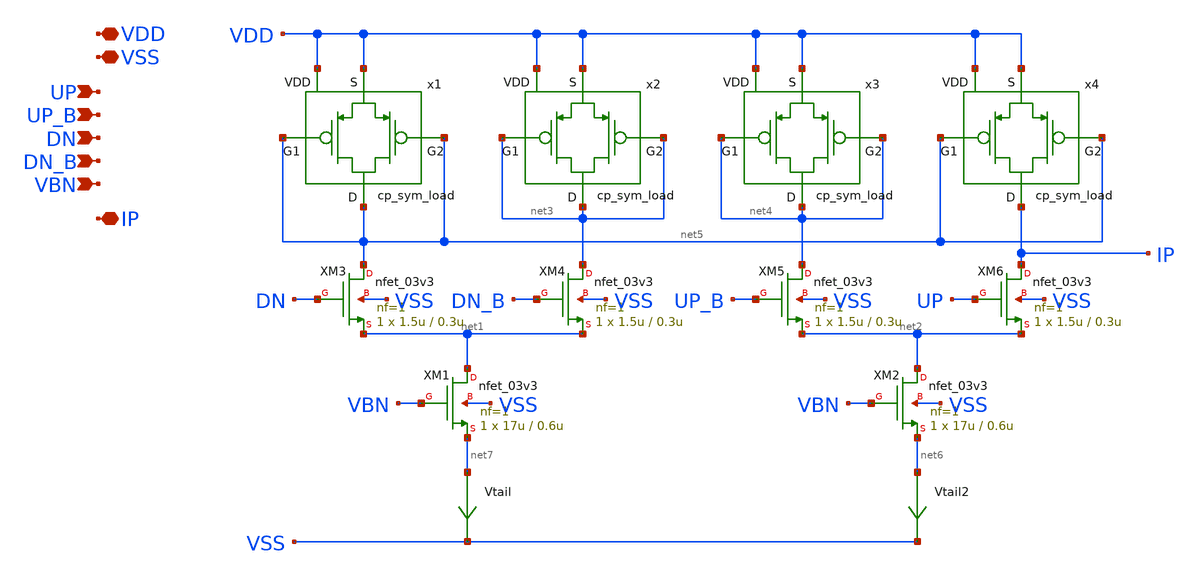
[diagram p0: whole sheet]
** sch_path: designs/libs/core_analog/charge_pump/charge_pump.sch
**.subckt charge_pump VDD VSS UP UP_B DN DN_B VBN IP
*.iopin VDD
*.iopin VSS
*.ipin UP
*.ipin UP_B
*.ipin DN
*.ipin DN_B
*.ipin VBN
*.iopin IP
XM1 net1 VBN net7 VSS nfet_03v3 L=0.6u W=17u nf=1 ad='int((nf+1)/2) * W/nf * 0.18u' as='int((nf+2)/2) * W/nf * 0.18u'
+ pd='2*int((nf+1)/2) * (W/nf + 0.18u)' ps='2*int((nf+2)/2) * (W/nf + 0.18u)' nrd='0.18u / W' nrs='0.18u / W'
+ sa=0 sb=0 sd=0 m=1
XM2 net2 VBN net6 VSS nfet_03v3 L=0.6u W=17u nf=1 ad='int((nf+1)/2) * W/nf * 0.18u' as='int((nf+2)/2) * W/nf * 0.18u'
+ pd='2*int((nf+1)/2) * (W/nf + 0.18u)' ps='2*int((nf+2)/2) * (W/nf + 0.18u)' nrd='0.18u / W' nrs='0.18u / W'
+ sa=0 sb=0 sd=0 m=1
XM3 net5 DN net1 VSS nfet_03v3 L=0.3u W=1.5u nf=1 ad='int((nf+1)/2) * W/nf * 0.18u' as='int((nf+2)/2) * W/nf * 0.18u'
+ pd='2*int((nf+1)/2) * (W/nf + 0.18u)' ps='2*int((nf+2)/2) * (W/nf + 0.18u)' nrd='0.18u / W' nrs='0.18u / W'
+ sa=0 sb=0 sd=0 m=1
XM4 net3 DN_B net1 VSS nfet_03v3 L=0.3u W=1.5u nf=1 ad='int((nf+1)/2) * W/nf * 0.18u' as='int((nf+2)/2) * W/nf * 0.18u'
+ pd='2*int((nf+1)/2) * (W/nf + 0.18u)' ps='2*int((nf+2)/2) * (W/nf + 0.18u)' nrd='0.18u / W' nrs='0.18u / W'
+ sa=0 sb=0 sd=0 m=1
XM5 net4 UP_B net2 VSS nfet_03v3 L=0.3u W=1.5u nf=1 ad='int((nf+1)/2) * W/nf * 0.18u' as='int((nf+2)/2) * W/nf * 0.18u'
+ pd='2*int((nf+1)/2) * (W/nf + 0.18u)' ps='2*int((nf+2)/2) * (W/nf + 0.18u)' nrd='0.18u / W' nrs='0.18u / W'
+ sa=0 sb=0 sd=0 m=1
XM6 IP UP net2 VSS nfet_03v3 L=0.3u W=1.5u nf=1 ad='int((nf+1)/2) * W/nf * 0.18u' as='int((nf+2)/2) * W/nf * 0.18u'
+ pd='2*int((nf+1)/2) * (W/nf + 0.18u)' ps='2*int((nf+2)/2) * (W/nf + 0.18u)' nrd='0.18u / W' nrs='0.18u / W'
+ sa=0 sb=0 sd=0 m=1
x1 net5 net5 VDD net5 VDD cp_sym_load
x2 net3 net3 VDD net3 VDD cp_sym_load
x3 net4 net4 VDD net4 VDD cp_sym_load
x4 net5 net5 VDD IP VDD cp_sym_load
Vtail net7 VSS 0
.save i(vtail)
Vtail2 net6 VSS 0
.save i(vtail2)
**.ends

* expanding   symbol:
*+  /foss/designs/synchronos-chipathon-2026/designs/libs/core_analog/cp_sym_load/cp_sym_load.sym # of pins=5
** sym_path: designs/libs/core_analog/cp_sym_load/cp_sym_load.sym
** sch_path: designs/libs/core_analog/cp_sym_load/cp_sym_load.sch
.subckt cp_sym_load G1 G2 S D VDD
*.ipin G1
*.ipin G2
*.iopin S
*.iopin D
*.iopin VDD
XM1 D G1 S VDD pfet_03v3 L=0.3u W=1.5u nf=1 ad='int((nf+1)/2) * W/nf * 0.18u' as='int((nf+2)/2) * W/nf * 0.18u'
+ pd='2*int((nf+1)/2) * (W/nf + 0.18u)' ps='2*int((nf+2)/2) * (W/nf + 0.18u)' nrd='0.18u / W' nrs='0.18u / W'
+ sa=0 sb=0 sd=0 m=1
XM2 D G2 S VDD pfet_03v3 L=0.3u W=1.5u nf=1 ad='int((nf+1)/2) * W/nf * 0.18u' as='int((nf+2)/2) * W/nf * 0.18u'
+ pd='2*int((nf+1)/2) * (W/nf + 0.18u)' ps='2*int((nf+2)/2) * (W/nf + 0.18u)' nrd='0.18u / W' nrs='0.18u / W'
+ sa=0 sb=0 sd=0 m=1
.ends

.end
